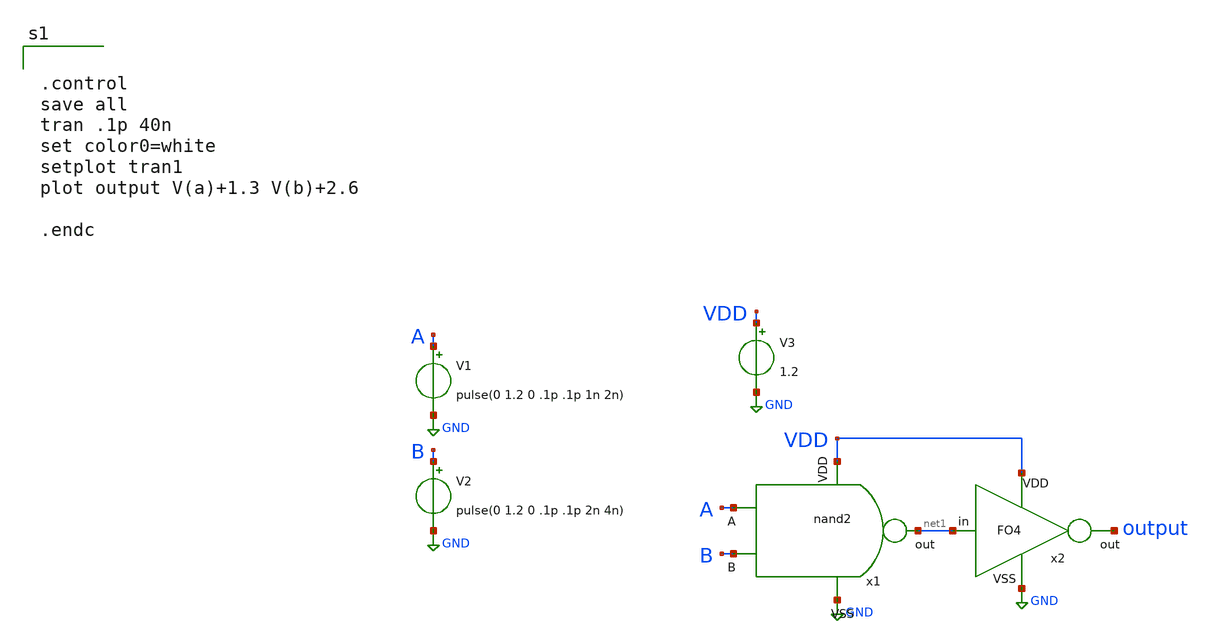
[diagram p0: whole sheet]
** sch_path: nand/nand2_tb.sch
**.subckt nand2_tb
V1 A GND pulse(0 1.2 0 .1p .1p 1n 2n)
V2 B GND pulse(0 1.2 0 .1p .1p 2n 4n)
V3 VDD GND 1.2
x2 VDD GND net1 output FO4
x1 VDD A B net1 GND nand2
**** begin user architecture code

** opencircuitdesign pdks install
.lib $::SKYWATER_MODELS/sky130.lib.spice tt




.control
save all
tran .1p 40n
set color0=white
setplot tran1
plot output V(a)+1.3 V(b)+2.6

.endc

**** end user architecture code
**.ends

* expanding   symbol:  FO4/FO4.sym # of pins=4
** sym_path: FO4/FO4.sym
** sch_path: FO4/FO4.sch
.subckt FO4 VDD VSS in out
*.ipin VDD
*.ipin VSS
*.ipin in
*.opin out
XM1 net1 in VSS VSS sky130_fd_pr__nfet_01v8 L=0.15 W=0.7 nf=1 ad='int((nf+1)/2) * W/nf * 0.29' as='int((nf+2)/2) * W/nf * 0.29'
+ pd='2*int((nf+1)/2) * (W/nf + 0.29)' ps='2*int((nf+2)/2) * (W/nf + 0.29)' nrd='0.29 / W' nrs='0.29 / W'
+ sa=0 sb=0 sd=0 mult=1 m=1
XM2 net1 in VDD VDD sky130_fd_pr__pfet_01v8 L=0.15 W=1 nf=1 ad='int((nf+1)/2) * W/nf * 0.29' as='int((nf+2)/2) * W/nf * 0.29'
+ pd='2*int((nf+1)/2) * (W/nf + 0.29)' ps='2*int((nf+2)/2) * (W/nf + 0.29)' nrd='0.29 / W' nrs='0.29 / W'
+ sa=0 sb=0 sd=0 mult=1 m=1
XM3 net2 in VSS VSS sky130_fd_pr__nfet_01v8 L=0.15 W=0.7 nf=1 ad='int((nf+1)/2) * W/nf * 0.29' as='int((nf+2)/2) * W/nf * 0.29'
+ pd='2*int((nf+1)/2) * (W/nf + 0.29)' ps='2*int((nf+2)/2) * (W/nf + 0.29)' nrd='0.29 / W' nrs='0.29 / W'
+ sa=0 sb=0 sd=0 mult=1 m=1
XM4 net2 in VDD VDD sky130_fd_pr__pfet_01v8 L=0.15 W=1 nf=1 ad='int((nf+1)/2) * W/nf * 0.29' as='int((nf+2)/2) * W/nf * 0.29'
+ pd='2*int((nf+1)/2) * (W/nf + 0.29)' ps='2*int((nf+2)/2) * (W/nf + 0.29)' nrd='0.29 / W' nrs='0.29 / W'
+ sa=0 sb=0 sd=0 mult=1 m=1
XM5 net3 in VSS VSS sky130_fd_pr__nfet_01v8 L=0.15 W=0.7 nf=1 ad='int((nf+1)/2) * W/nf * 0.29' as='int((nf+2)/2) * W/nf * 0.29'
+ pd='2*int((nf+1)/2) * (W/nf + 0.29)' ps='2*int((nf+2)/2) * (W/nf + 0.29)' nrd='0.29 / W' nrs='0.29 / W'
+ sa=0 sb=0 sd=0 mult=1 m=1
XM6 net3 in VDD VDD sky130_fd_pr__pfet_01v8 L=0.15 W=1 nf=1 ad='int((nf+1)/2) * W/nf * 0.29' as='int((nf+2)/2) * W/nf * 0.29'
+ pd='2*int((nf+1)/2) * (W/nf + 0.29)' ps='2*int((nf+2)/2) * (W/nf + 0.29)' nrd='0.29 / W' nrs='0.29 / W'
+ sa=0 sb=0 sd=0 mult=1 m=1
XM7 out in VSS VSS sky130_fd_pr__nfet_01v8 L=0.15 W=0.7 nf=1 ad='int((nf+1)/2) * W/nf * 0.29' as='int((nf+2)/2) * W/nf * 0.29'
+ pd='2*int((nf+1)/2) * (W/nf + 0.29)' ps='2*int((nf+2)/2) * (W/nf + 0.29)' nrd='0.29 / W' nrs='0.29 / W'
+ sa=0 sb=0 sd=0 mult=1 m=1
XM8 out in VDD VDD sky130_fd_pr__pfet_01v8 L=0.15 W=1 nf=1 ad='int((nf+1)/2) * W/nf * 0.29' as='int((nf+2)/2) * W/nf * 0.29'
+ pd='2*int((nf+1)/2) * (W/nf + 0.29)' ps='2*int((nf+2)/2) * (W/nf + 0.29)' nrd='0.29 / W' nrs='0.29 / W'
+ sa=0 sb=0 sd=0 mult=1 m=1
.ends


* expanding   symbol:  nand/nand2.sym # of pins=5
** sym_path: nand/nand2.sym
** sch_path: nand/nand2.sch
.subckt nand2 VDD A B out VSS
*.ipin VDD
*.ipin A
*.ipin B
*.ipin VSS
*.opin out
XM1 out A net1 net1 sky130_fd_pr__nfet_01v8 L=0.15 W=10 nf=1 ad='int((nf+1)/2) * W/nf * 0.29' as='int((nf+2)/2) * W/nf * 0.29'
+ pd='2*int((nf+1)/2) * (W/nf + 0.29)' ps='2*int((nf+2)/2) * (W/nf + 0.29)' nrd='0.29 / W' nrs='0.29 / W'
+ sa=0 sb=0 sd=0 mult=1 m=1
XM2 out A VDD VDD sky130_fd_pr__pfet_01v8 L=0.15 W=10 nf=1 ad='int((nf+1)/2) * W/nf * 0.29' as='int((nf+2)/2) * W/nf * 0.29'
+ pd='2*int((nf+1)/2) * (W/nf + 0.29)' ps='2*int((nf+2)/2) * (W/nf + 0.29)' nrd='0.29 / W' nrs='0.29 / W'
+ sa=0 sb=0 sd=0 mult=1 m=1
XM3 net1 B VSS VSS sky130_fd_pr__nfet_01v8 L=0.15 W=10 nf=1 ad='int((nf+1)/2) * W/nf * 0.29' as='int((nf+2)/2) * W/nf * 0.29'
+ pd='2*int((nf+1)/2) * (W/nf + 0.29)' ps='2*int((nf+2)/2) * (W/nf + 0.29)' nrd='0.29 / W' nrs='0.29 / W'
+ sa=0 sb=0 sd=0 mult=1 m=1
XM4 out B VDD VDD sky130_fd_pr__pfet_01v8 L=0.15 W=10 nf=1 ad='int((nf+1)/2) * W/nf * 0.29' as='int((nf+2)/2) * W/nf * 0.29'
+ pd='2*int((nf+1)/2) * (W/nf + 0.29)' ps='2*int((nf+2)/2) * (W/nf + 0.29)' nrd='0.29 / W' nrs='0.29 / W'
+ sa=0 sb=0 sd=0 mult=1 m=1
.ends

.GLOBAL GND
.end
